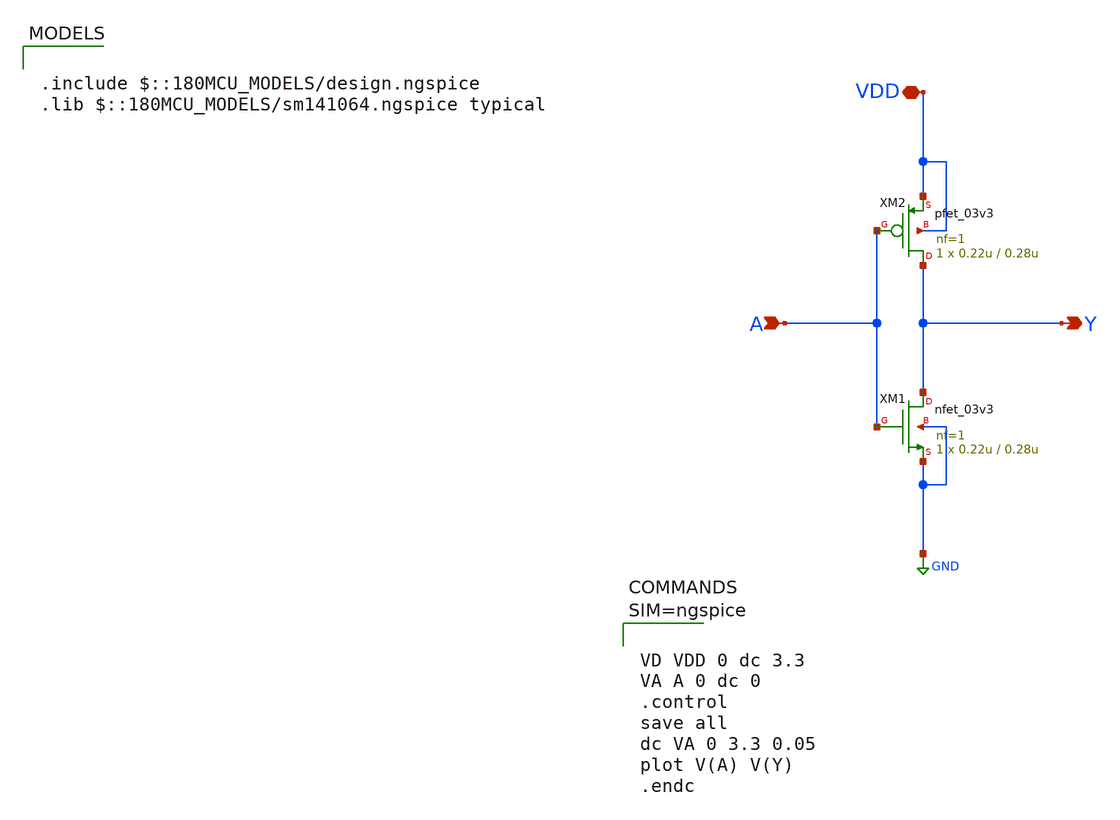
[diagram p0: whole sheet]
** sch_path: xschem/inverter_tb.sch
**.subckt inverter_tb Y A VDD
*.opin Y
*.ipin A
*.iopin VDD
XM1 Y A GND GND nfet_03v3 L=0.28u W=0.22u nf=1 ad='int((nf+1)/2) * W/nf * 0.18u' as='int((nf+2)/2) * W/nf * 0.18u'
+ pd='2*int((nf+1)/2) * (W/nf + 0.18u)' ps='2*int((nf+2)/2) * (W/nf + 0.18u)' nrd='0.18u / W' nrs='0.18u / W'
+ sa=0 sb=0 sd=0 m=1
XM2 Y A VDD VDD pfet_03v3 L=0.28u W=0.22u nf=1 ad='int((nf+1)/2) * W/nf * 0.18u' as='int((nf+2)/2) * W/nf * 0.18u'
+ pd='2*int((nf+1)/2) * (W/nf + 0.18u)' ps='2*int((nf+2)/2) * (W/nf + 0.18u)' nrd='0.18u / W' nrs='0.18u / W'
+ sa=0 sb=0 sd=0 m=1
**** begin user architecture code

.include $::180MCU_MODELS/design.ngspice
.lib $::180MCU_MODELS/sm141064.ngspice typical




VD VDD 0 dc 3.3
VA A 0 dc 0
.control
save all
dc VA 0 3.3 0.05
plot V(A) V(Y)
.endc



**** end user architecture code
**.ends
.GLOBAL GND
.end
